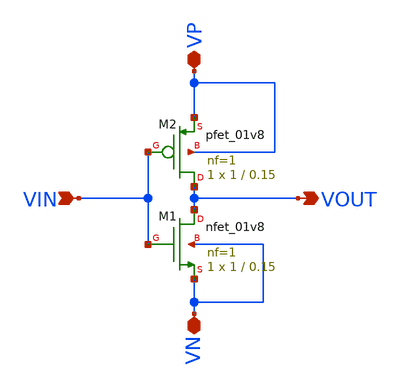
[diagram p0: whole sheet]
** sch_path: xschem/inverter_1.sch
**.subckt inverter_1 VIN VN VP VOUT
*.ipin VIN
*.iopin VN
*.iopin VP
*.opin VOUT
XM1 VOUT VIN VN VN sky130_fd_pr__nfet_01v8 L=0.15 W=1 nf=1 ad='int((nf+1)/2) * W/nf * 0.29' as='int((nf+2)/2) * W/nf * 0.29'
+ pd='2*int((nf+1)/2) * (W/nf + 0.29)' ps='2*int((nf+2)/2) * (W/nf + 0.29)' nrd='0.29 / W' nrs='0.29 / W'
+ sa=0 sb=0 sd=0 mult=1 m=1
XM2 VOUT VIN VP VP sky130_fd_pr__pfet_01v8 L=0.15 W=1 nf=1 ad='int((nf+1)/2) * W/nf * 0.29' as='int((nf+2)/2) * W/nf * 0.29'
+ pd='2*int((nf+1)/2) * (W/nf + 0.29)' ps='2*int((nf+2)/2) * (W/nf + 0.29)' nrd='0.29 / W' nrs='0.29 / W'
+ sa=0 sb=0 sd=0 mult=1 m=1
**.ends
.end
